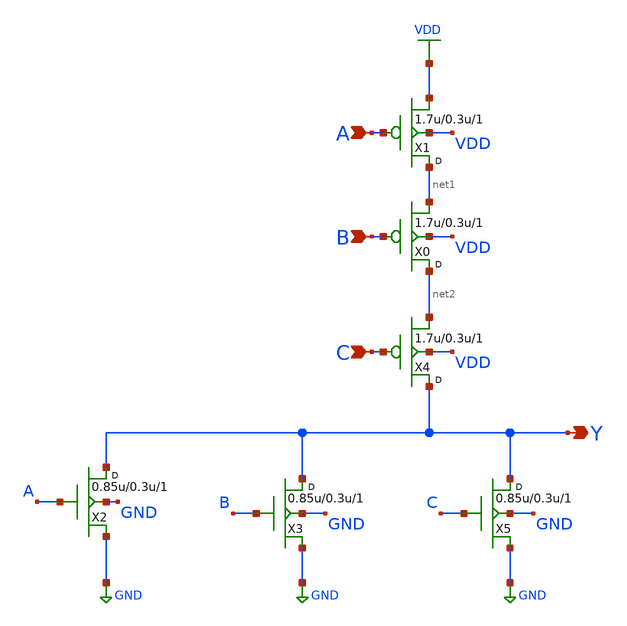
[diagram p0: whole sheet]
** sch_path: designs/libs/core_digital/gf180mcu_osu_sc_gp12t3v3/cells/nor3/gf180mcu_osu_sc_gp12t3v3__nor3_1.sch
**.subckt gf180mcu_osu_sc_gp12t3v3__nor3_1 A B Y C
*.ipin A
*.ipin B
*.opin Y
*.ipin C
X1 net1 A VDD VDD pfet_03v3 w=1.7u l=0.3u m=1
X0 net2 B net1 VDD pfet_03v3 w=1.7u l=0.3u m=1
X2 Y A GND GND nfet_03v3 w=0.85u l=0.3u m=1
X3 Y B GND GND nfet_03v3 w=0.85u l=0.3u m=1
X4 Y C net2 VDD pfet_03v3 w=1.7u l=0.3u m=1
X5 Y C GND GND nfet_03v3 w=0.85u l=0.3u m=1
**.ends
.GLOBAL VDD
.GLOBAL GND
.end
